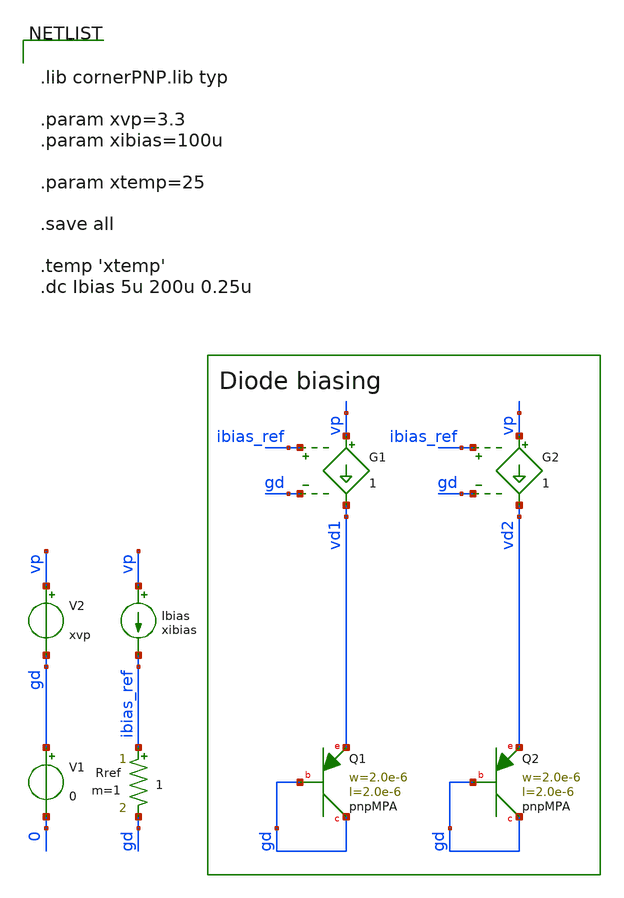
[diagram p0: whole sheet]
** sch_path: testbench/ip_bandgap_delta_v_tb.sch
**.subckt ip_bandgap_delta_v_tb
Ibias vp ibias_ref xibias
Rref ibias_ref gd 1 m=1
V1 gd 0 0
V2 vp gd xvp
XQ1 gd gd vd1 pnpMPA a=4p p=8u m=1
XQ2 gd gd vd2 pnpMPA a=4p p=8u m=8
G1 vp vd1 ibias_ref gd 1
G2 vp vd2 ibias_ref gd 1
**** begin user architecture code


.lib cornerPNP.lib typ

.param xvp=3.3
.param xibias=100u

.param xtemp=25

.save all

.temp 'xtemp'
.dc Ibias 5u 200u 0.25u


**** end user architecture code
**.ends
.end
